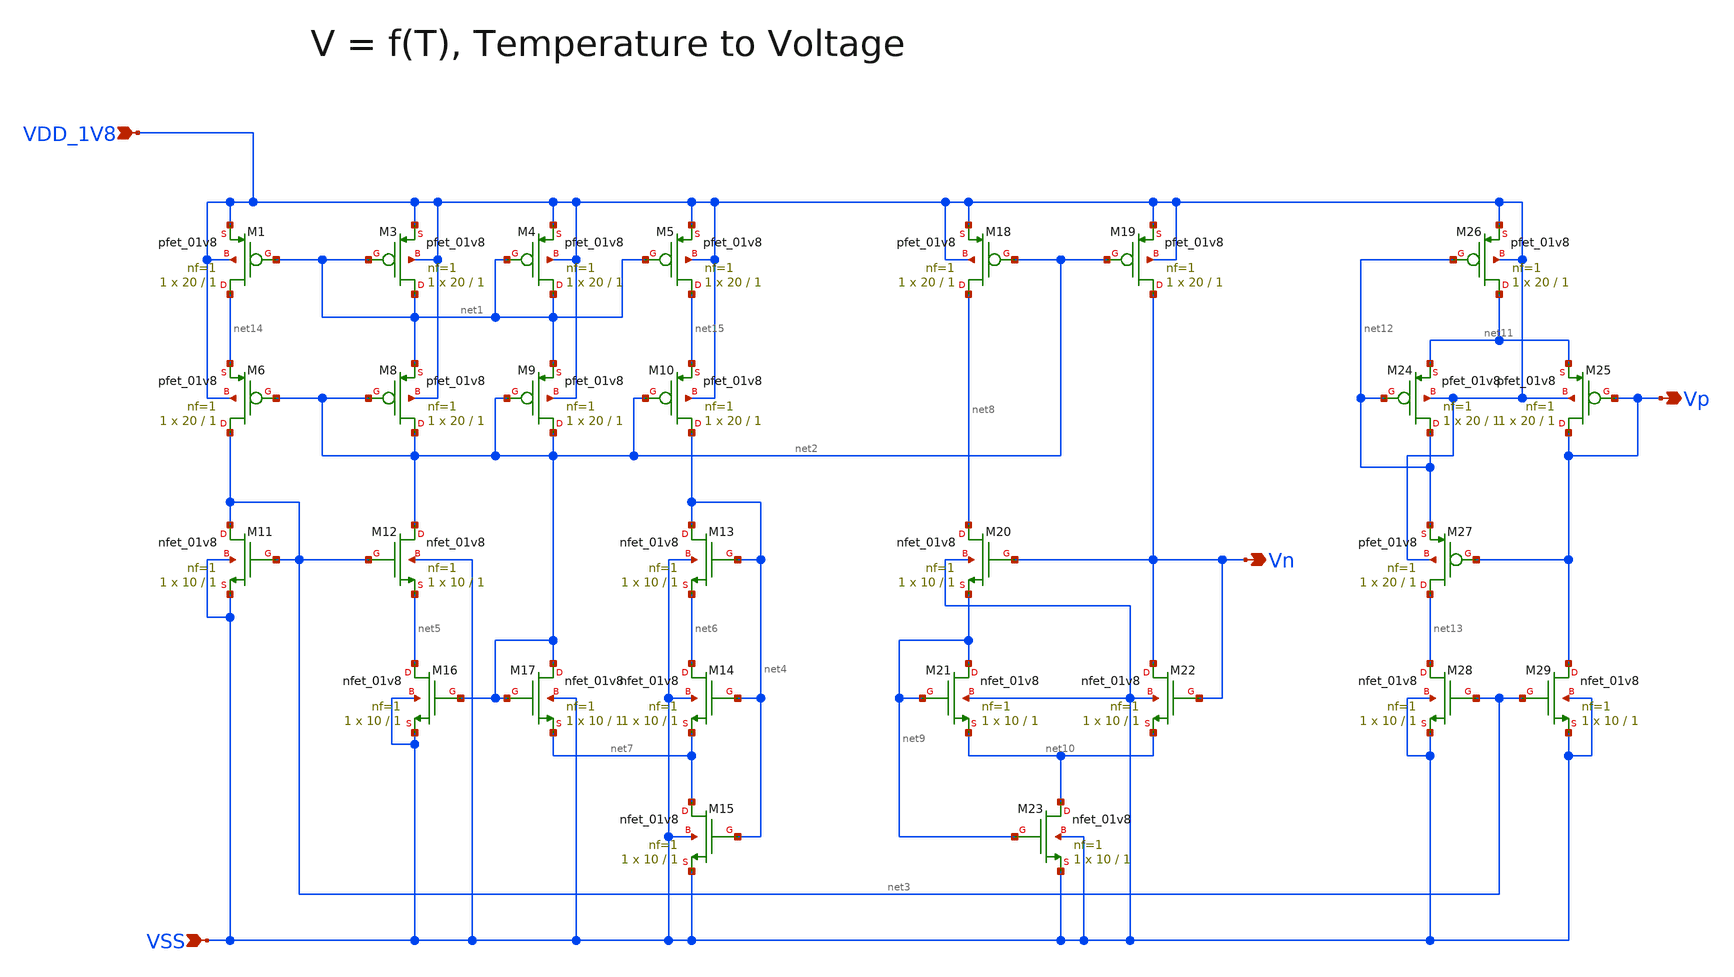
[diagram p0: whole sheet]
** sch_path: design/CNR_GR06_SKY130NM/CNR_GR06_test.sch
**.subckt CNR_GR06_test VSS Vn Vp VDD_1V8
*.ipin VSS
*.opin Vn
*.opin Vp
*.ipin VDD_1V8
XM1 net14 net1 VDD_1V8 VDD_1V8 sky130_fd_pr__pfet_01v8 L=1 W=20 nf=1 ad='int((nf+1)/2) * W/nf * 0.29'
+ as='int((nf+2)/2) * W/nf * 0.29' pd='2*int((nf+1)/2) * (W/nf + 0.29)' ps='2*int((nf+2)/2) * (W/nf + 0.29)'
+ nrd='0.29 / W' nrs='0.29 / W' sa=0 sb=0 sd=0 mult=1 m=1
XM3 net1 net1 VDD_1V8 VDD_1V8 sky130_fd_pr__pfet_01v8 L=1 W=20 nf=1 ad='int((nf+1)/2) * W/nf * 0.29'
+ as='int((nf+2)/2) * W/nf * 0.29' pd='2*int((nf+1)/2) * (W/nf + 0.29)' ps='2*int((nf+2)/2) * (W/nf + 0.29)'
+ nrd='0.29 / W' nrs='0.29 / W' sa=0 sb=0 sd=0 mult=1 m=1
XM4 net1 net1 VDD_1V8 VDD_1V8 sky130_fd_pr__pfet_01v8 L=1 W=20 nf=1 ad='int((nf+1)/2) * W/nf * 0.29'
+ as='int((nf+2)/2) * W/nf * 0.29' pd='2*int((nf+1)/2) * (W/nf + 0.29)' ps='2*int((nf+2)/2) * (W/nf + 0.29)'
+ nrd='0.29 / W' nrs='0.29 / W' sa=0 sb=0 sd=0 mult=1 m=1
XM5 net15 net1 VDD_1V8 VDD_1V8 sky130_fd_pr__pfet_01v8 L=1 W=20 nf=1 ad='int((nf+1)/2) * W/nf * 0.29'
+ as='int((nf+2)/2) * W/nf * 0.29' pd='2*int((nf+1)/2) * (W/nf + 0.29)' ps='2*int((nf+2)/2) * (W/nf + 0.29)'
+ nrd='0.29 / W' nrs='0.29 / W' sa=0 sb=0 sd=0 mult=1 m=1
XM6 net3 net2 net14 VDD_1V8 sky130_fd_pr__pfet_01v8 L=1 W=20 nf=1 ad='int((nf+1)/2) * W/nf * 0.29' as='int((nf+2)/2) * W/nf * 0.29'
+ pd='2*int((nf+1)/2) * (W/nf + 0.29)' ps='2*int((nf+2)/2) * (W/nf + 0.29)' nrd='0.29 / W' nrs='0.29 / W'
+ sa=0 sb=0 sd=0 mult=1 m=1
XM8 net2 net2 net1 VDD_1V8 sky130_fd_pr__pfet_01v8 L=1 W=20 nf=1 ad='int((nf+1)/2) * W/nf * 0.29' as='int((nf+2)/2) * W/nf * 0.29'
+ pd='2*int((nf+1)/2) * (W/nf + 0.29)' ps='2*int((nf+2)/2) * (W/nf + 0.29)' nrd='0.29 / W' nrs='0.29 / W'
+ sa=0 sb=0 sd=0 mult=1 m=1
XM9 net2 net2 net1 VDD_1V8 sky130_fd_pr__pfet_01v8 L=1 W=20 nf=1 ad='int((nf+1)/2) * W/nf * 0.29' as='int((nf+2)/2) * W/nf * 0.29'
+ pd='2*int((nf+1)/2) * (W/nf + 0.29)' ps='2*int((nf+2)/2) * (W/nf + 0.29)' nrd='0.29 / W' nrs='0.29 / W'
+ sa=0 sb=0 sd=0 mult=1 m=1
XM10 net4 net2 net15 VDD_1V8 sky130_fd_pr__pfet_01v8 L=1 W=20 nf=1 ad='int((nf+1)/2) * W/nf * 0.29' as='int((nf+2)/2) * W/nf * 0.29'
+ pd='2*int((nf+1)/2) * (W/nf + 0.29)' ps='2*int((nf+2)/2) * (W/nf + 0.29)' nrd='0.29 / W' nrs='0.29 / W'
+ sa=0 sb=0 sd=0 mult=1 m=1
XM11 net3 net3 VSS VSS sky130_fd_pr__nfet_01v8 L=1 W=10 nf=1 ad='int((nf+1)/2) * W/nf * 0.29' as='int((nf+2)/2) * W/nf * 0.29'
+ pd='2*int((nf+1)/2) * (W/nf + 0.29)' ps='2*int((nf+2)/2) * (W/nf + 0.29)' nrd='0.29 / W' nrs='0.29 / W'
+ sa=0 sb=0 sd=0 mult=1 m=1
XM12 net2 net3 net5 VSS sky130_fd_pr__nfet_01v8 L=1 W=10 nf=1 ad='int((nf+1)/2) * W/nf * 0.29' as='int((nf+2)/2) * W/nf * 0.29'
+ pd='2*int((nf+1)/2) * (W/nf + 0.29)' ps='2*int((nf+2)/2) * (W/nf + 0.29)' nrd='0.29 / W' nrs='0.29 / W'
+ sa=0 sb=0 sd=0 mult=1 m=1
XM13 net4 net4 net6 VSS sky130_fd_pr__nfet_01v8 L=1 W=10 nf=1 ad='int((nf+1)/2) * W/nf * 0.29' as='int((nf+2)/2) * W/nf * 0.29'
+ pd='2*int((nf+1)/2) * (W/nf + 0.29)' ps='2*int((nf+2)/2) * (W/nf + 0.29)' nrd='0.29 / W' nrs='0.29 / W'
+ sa=0 sb=0 sd=0 mult=1 m=1
XM14 net6 net4 net7 VSS sky130_fd_pr__nfet_01v8 L=1 W=10 nf=1 ad='int((nf+1)/2) * W/nf * 0.29' as='int((nf+2)/2) * W/nf * 0.29'
+ pd='2*int((nf+1)/2) * (W/nf + 0.29)' ps='2*int((nf+2)/2) * (W/nf + 0.29)' nrd='0.29 / W' nrs='0.29 / W'
+ sa=0 sb=0 sd=0 mult=1 m=1
XM15 net7 net4 VSS VSS sky130_fd_pr__nfet_01v8 L=1 W=10 nf=1 ad='int((nf+1)/2) * W/nf * 0.29' as='int((nf+2)/2) * W/nf * 0.29'
+ pd='2*int((nf+1)/2) * (W/nf + 0.29)' ps='2*int((nf+2)/2) * (W/nf + 0.29)' nrd='0.29 / W' nrs='0.29 / W'
+ sa=0 sb=0 sd=0 mult=1 m=1
XM16 net5 net2 VSS VSS sky130_fd_pr__nfet_01v8 L=1 W=10 nf=1 ad='int((nf+1)/2) * W/nf * 0.29' as='int((nf+2)/2) * W/nf * 0.29'
+ pd='2*int((nf+1)/2) * (W/nf + 0.29)' ps='2*int((nf+2)/2) * (W/nf + 0.29)' nrd='0.29 / W' nrs='0.29 / W'
+ sa=0 sb=0 sd=0 mult=1 m=1
XM17 net2 net2 net7 VSS sky130_fd_pr__nfet_01v8 L=1 W=10 nf=1 ad='int((nf+1)/2) * W/nf * 0.29' as='int((nf+2)/2) * W/nf * 0.29'
+ pd='2*int((nf+1)/2) * (W/nf + 0.29)' ps='2*int((nf+2)/2) * (W/nf + 0.29)' nrd='0.29 / W' nrs='0.29 / W'
+ sa=0 sb=0 sd=0 mult=1 m=1
XM18 net8 net2 VDD_1V8 VDD_1V8 sky130_fd_pr__pfet_01v8 L=1 W=20 nf=1 ad='int((nf+1)/2) * W/nf * 0.29'
+ as='int((nf+2)/2) * W/nf * 0.29' pd='2*int((nf+1)/2) * (W/nf + 0.29)' ps='2*int((nf+2)/2) * (W/nf + 0.29)'
+ nrd='0.29 / W' nrs='0.29 / W' sa=0 sb=0 sd=0 mult=1 m=1
XM19 Vn net2 VDD_1V8 VDD_1V8 sky130_fd_pr__pfet_01v8 L=1 W=20 nf=1 ad='int((nf+1)/2) * W/nf * 0.29' as='int((nf+2)/2) * W/nf * 0.29'
+ pd='2*int((nf+1)/2) * (W/nf + 0.29)' ps='2*int((nf+2)/2) * (W/nf + 0.29)' nrd='0.29 / W' nrs='0.29 / W'
+ sa=0 sb=0 sd=0 mult=1 m=1
XM20 net8 Vn net9 VSS sky130_fd_pr__nfet_01v8 L=1 W=10 nf=1 ad='int((nf+1)/2) * W/nf * 0.29' as='int((nf+2)/2) * W/nf * 0.29'
+ pd='2*int((nf+1)/2) * (W/nf + 0.29)' ps='2*int((nf+2)/2) * (W/nf + 0.29)' nrd='0.29 / W' nrs='0.29 / W'
+ sa=0 sb=0 sd=0 mult=1 m=1
XM21 net9 net9 net10 VSS sky130_fd_pr__nfet_01v8 L=1 W=10 nf=1 ad='int((nf+1)/2) * W/nf * 0.29' as='int((nf+2)/2) * W/nf * 0.29'
+ pd='2*int((nf+1)/2) * (W/nf + 0.29)' ps='2*int((nf+2)/2) * (W/nf + 0.29)' nrd='0.29 / W' nrs='0.29 / W'
+ sa=0 sb=0 sd=0 mult=1 m=1
XM22 Vn Vn net10 VSS sky130_fd_pr__nfet_01v8 L=1 W=10 nf=1 ad='int((nf+1)/2) * W/nf * 0.29' as='int((nf+2)/2) * W/nf * 0.29'
+ pd='2*int((nf+1)/2) * (W/nf + 0.29)' ps='2*int((nf+2)/2) * (W/nf + 0.29)' nrd='0.29 / W' nrs='0.29 / W'
+ sa=0 sb=0 sd=0 mult=1 m=1
XM23 net10 net9 VSS VSS sky130_fd_pr__nfet_01v8 L=1 W=10 nf=1 ad='int((nf+1)/2) * W/nf * 0.29' as='int((nf+2)/2) * W/nf * 0.29'
+ pd='2*int((nf+1)/2) * (W/nf + 0.29)' ps='2*int((nf+2)/2) * (W/nf + 0.29)' nrd='0.29 / W' nrs='0.29 / W'
+ sa=0 sb=0 sd=0 mult=1 m=1
XM24 net12 net12 net11 VDD_1V8 sky130_fd_pr__pfet_01v8 L=1 W=20 nf=1 ad='int((nf+1)/2) * W/nf * 0.29'
+ as='int((nf+2)/2) * W/nf * 0.29' pd='2*int((nf+1)/2) * (W/nf + 0.29)' ps='2*int((nf+2)/2) * (W/nf + 0.29)'
+ nrd='0.29 / W' nrs='0.29 / W' sa=0 sb=0 sd=0 mult=1 m=1
XM25 Vp Vp net11 VDD_1V8 sky130_fd_pr__pfet_01v8 L=1 W=20 nf=1 ad='int((nf+1)/2) * W/nf * 0.29' as='int((nf+2)/2) * W/nf * 0.29'
+ pd='2*int((nf+1)/2) * (W/nf + 0.29)' ps='2*int((nf+2)/2) * (W/nf + 0.29)' nrd='0.29 / W' nrs='0.29 / W'
+ sa=0 sb=0 sd=0 mult=1 m=1
XM26 net11 net12 VDD_1V8 VDD_1V8 sky130_fd_pr__pfet_01v8 L=1 W=20 nf=1 ad='int((nf+1)/2) * W/nf * 0.29'
+ as='int((nf+2)/2) * W/nf * 0.29' pd='2*int((nf+1)/2) * (W/nf + 0.29)' ps='2*int((nf+2)/2) * (W/nf + 0.29)'
+ nrd='0.29 / W' nrs='0.29 / W' sa=0 sb=0 sd=0 mult=1 m=1
XM27 net13 Vp net12 VDD_1V8 sky130_fd_pr__pfet_01v8 L=1 W=20 nf=1 ad='int((nf+1)/2) * W/nf * 0.29' as='int((nf+2)/2) * W/nf * 0.29'
+ pd='2*int((nf+1)/2) * (W/nf + 0.29)' ps='2*int((nf+2)/2) * (W/nf + 0.29)' nrd='0.29 / W' nrs='0.29 / W'
+ sa=0 sb=0 sd=0 mult=1 m=1
XM28 net13 net3 VSS VSS sky130_fd_pr__nfet_01v8 L=1 W=10 nf=1 ad='int((nf+1)/2) * W/nf * 0.29' as='int((nf+2)/2) * W/nf * 0.29'
+ pd='2*int((nf+1)/2) * (W/nf + 0.29)' ps='2*int((nf+2)/2) * (W/nf + 0.29)' nrd='0.29 / W' nrs='0.29 / W'
+ sa=0 sb=0 sd=0 mult=1 m=1
XM29 Vp net3 VSS VSS sky130_fd_pr__nfet_01v8 L=1 W=10 nf=1 ad='int((nf+1)/2) * W/nf * 0.29' as='int((nf+2)/2) * W/nf * 0.29'
+ pd='2*int((nf+1)/2) * (W/nf + 0.29)' ps='2*int((nf+2)/2) * (W/nf + 0.29)' nrd='0.29 / W' nrs='0.29 / W'
+ sa=0 sb=0 sd=0 mult=1 m=1
**.ends
.end
